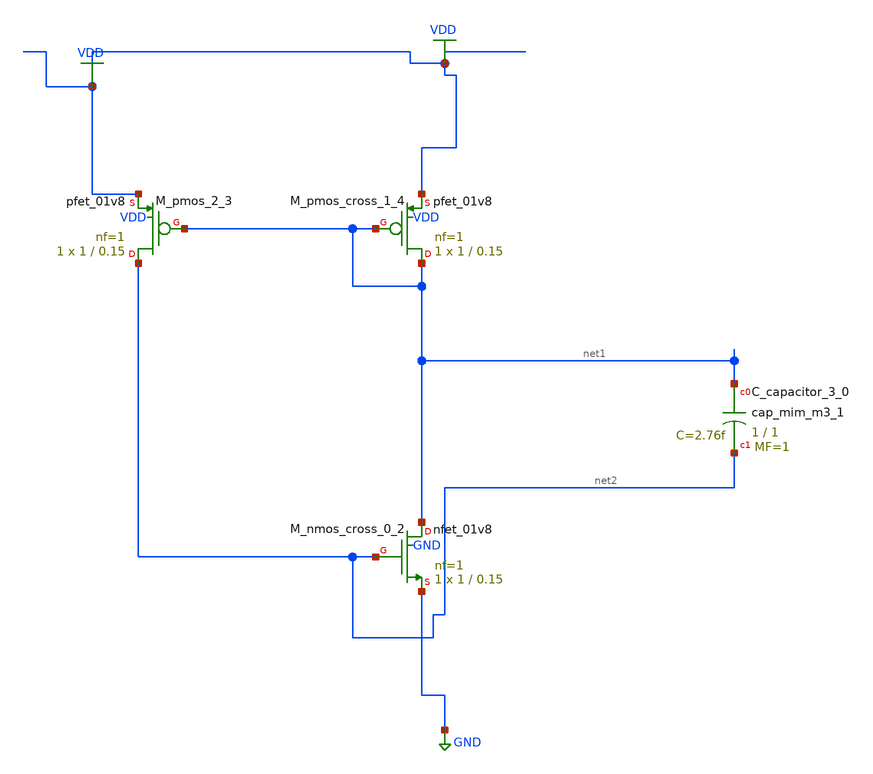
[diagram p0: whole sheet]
** sch_path: schematics/AMSNet/346.sch
**.subckt 346
XC_capacitor_3_0 net1 net2 sky130_fd_pr__cap_mim_m3_1 W=1 L=1 MF=1 m=1
XM_nmos_cross_0_2 net1 net2 GND GND sky130_fd_pr__nfet_01v8 L=0.15 W=1 nf=1 ad='int((1 + 1)/2) * 1 / 1 * 0.29'
+ as='int((1 + 2)/2) * 1 / 1 * 0.29' pd='2*int((1 + 1)/2) * (1 / 1 + 0.29)' ps='2*int((1 + 2)/2) * (1 / 1 + 0.29)'
+ nrd='0.29 / 1 ' nrs='0.29 / 1 ' sa=0 sb=0 sd=0 mult=1 m=1
XM_pmos_2_3 net2 net1 VDD VDD sky130_fd_pr__pfet_01v8 L=0.15 W=1 nf=1 ad='int((1 + 1)/2) * 1 / 1 * 0.29'
+ as='int((1 + 2)/2) * 1 / 1 * 0.29' pd='2*int((1 + 1)/2) * (1 / 1 + 0.29)' ps='2*int((1 + 2)/2) * (1 / 1 + 0.29)'
+ nrd='0.29 / 1 ' nrs='0.29 / 1 ' sa=0 sb=0 sd=0 mult=1 m=1
XM_pmos_cross_1_4 net1 net1 VDD VDD sky130_fd_pr__pfet_01v8 L=0.15 W=1 nf=1 ad='int((1 + 1)/2) * 1 / 1 * 0.29'
+ as='int((1 + 2)/2) * 1 / 1 * 0.29' pd='2*int((1 + 1)/2) * (1 / 1 + 0.29)' ps='2*int((1 + 2)/2) * (1 / 1 + 0.29)'
+ nrd='0.29 / 1 ' nrs='0.29 / 1 ' sa=0 sb=0 sd=0 mult=1 m=1
**.ends
.GLOBAL GND
.GLOBAL VDD
.end
